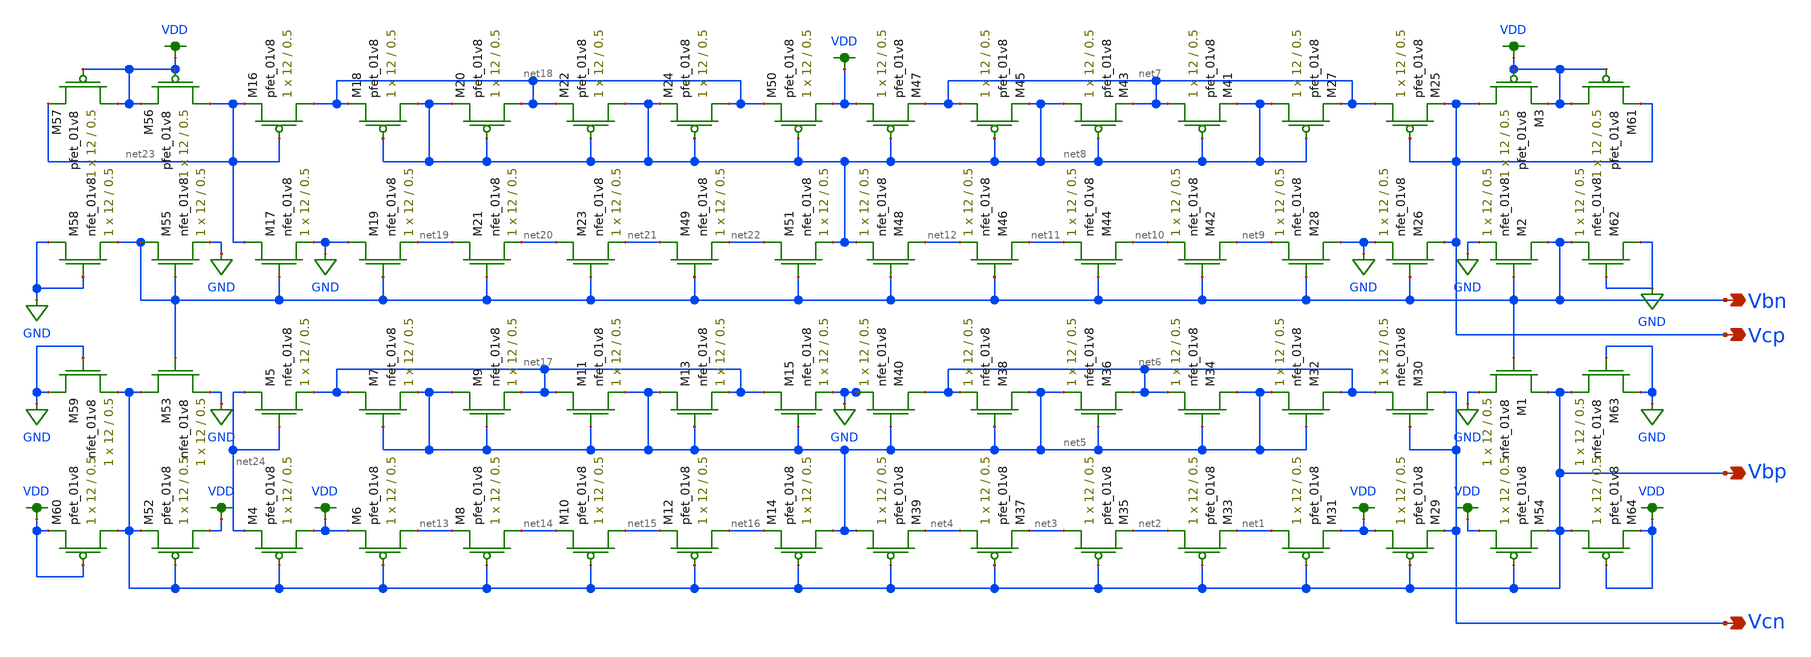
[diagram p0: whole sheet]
** sch_path: MP3/correction/xschem/v_gen_lds.sch
**.subckt v_gen_lds Vcp Vcn Vbn Vbp
*.opin Vcp
*.opin Vcn
*.opin Vbn
*.opin Vbp
XM29 VDD Vbp Vcn VDD sky130_fd_pr__pfet_01v8 L=0.5 W=12 nf=1 ad='int((nf+1)/2) * W/nf * 0.29' as='int((nf+2)/2) * W/nf * 0.29'
+ pd='2*int((nf+1)/2) * (W/nf + 0.29)' ps='2*int((nf+2)/2) * (W/nf + 0.29)' nrd='0.29 / W' nrs='0.29 / W'
+ sa=0 sb=0 sd=0 mult=1 m=1
XM30 Vcn Vcn net6 GND sky130_fd_pr__nfet_01v8 L=0.5 W=12 nf=1 ad='int((nf+1)/2) * W/nf * 0.29' as='int((nf+2)/2) * W/nf * 0.29'
+ pd='2*int((nf+1)/2) * (W/nf + 0.29)' ps='2*int((nf+2)/2) * (W/nf + 0.29)' nrd='0.29 / W' nrs='0.29 / W'
+ sa=0 sb=0 sd=0 mult=1 m=1
XM31 net1 Vbp VDD VDD sky130_fd_pr__pfet_01v8 L=0.5 W=12 nf=1 ad='int((nf+1)/2) * W/nf * 0.29' as='int((nf+2)/2) * W/nf * 0.29'
+ pd='2*int((nf+1)/2) * (W/nf + 0.29)' ps='2*int((nf+2)/2) * (W/nf + 0.29)' nrd='0.29 / W' nrs='0.29 / W'
+ sa=0 sb=0 sd=0 mult=1 m=1
XM32 net6 net5 net5 GND sky130_fd_pr__nfet_01v8 L=0.5 W=12 nf=1 ad='int((nf+1)/2) * W/nf * 0.29' as='int((nf+2)/2) * W/nf * 0.29'
+ pd='2*int((nf+1)/2) * (W/nf + 0.29)' ps='2*int((nf+2)/2) * (W/nf + 0.29)' nrd='0.29 / W' nrs='0.29 / W'
+ sa=0 sb=0 sd=0 mult=1 m=1
XM33 net2 Vbp net1 VDD sky130_fd_pr__pfet_01v8 L=0.5 W=12 nf=1 ad='int((nf+1)/2) * W/nf * 0.29' as='int((nf+2)/2) * W/nf * 0.29'
+ pd='2*int((nf+1)/2) * (W/nf + 0.29)' ps='2*int((nf+2)/2) * (W/nf + 0.29)' nrd='0.29 / W' nrs='0.29 / W'
+ sa=0 sb=0 sd=0 mult=1 m=1
XM34 net5 net5 net6 GND sky130_fd_pr__nfet_01v8 L=0.5 W=12 nf=1 ad='int((nf+1)/2) * W/nf * 0.29' as='int((nf+2)/2) * W/nf * 0.29'
+ pd='2*int((nf+1)/2) * (W/nf + 0.29)' ps='2*int((nf+2)/2) * (W/nf + 0.29)' nrd='0.29 / W' nrs='0.29 / W'
+ sa=0 sb=0 sd=0 mult=1 m=1
XM35 net3 Vbp net2 VDD sky130_fd_pr__pfet_01v8 L=0.5 W=12 nf=1 ad='int((nf+1)/2) * W/nf * 0.29' as='int((nf+2)/2) * W/nf * 0.29'
+ pd='2*int((nf+1)/2) * (W/nf + 0.29)' ps='2*int((nf+2)/2) * (W/nf + 0.29)' nrd='0.29 / W' nrs='0.29 / W'
+ sa=0 sb=0 sd=0 mult=1 m=1
XM36 net6 net5 net5 GND sky130_fd_pr__nfet_01v8 L=0.5 W=12 nf=1 ad='int((nf+1)/2) * W/nf * 0.29' as='int((nf+2)/2) * W/nf * 0.29'
+ pd='2*int((nf+1)/2) * (W/nf + 0.29)' ps='2*int((nf+2)/2) * (W/nf + 0.29)' nrd='0.29 / W' nrs='0.29 / W'
+ sa=0 sb=0 sd=0 mult=1 m=1
XM37 net4 Vbp net3 VDD sky130_fd_pr__pfet_01v8 L=0.5 W=12 nf=1 ad='int((nf+1)/2) * W/nf * 0.29' as='int((nf+2)/2) * W/nf * 0.29'
+ pd='2*int((nf+1)/2) * (W/nf + 0.29)' ps='2*int((nf+2)/2) * (W/nf + 0.29)' nrd='0.29 / W' nrs='0.29 / W'
+ sa=0 sb=0 sd=0 mult=1 m=1
XM38 net5 net5 net6 GND sky130_fd_pr__nfet_01v8 L=0.5 W=12 nf=1 ad='int((nf+1)/2) * W/nf * 0.29' as='int((nf+2)/2) * W/nf * 0.29'
+ pd='2*int((nf+1)/2) * (W/nf + 0.29)' ps='2*int((nf+2)/2) * (W/nf + 0.29)' nrd='0.29 / W' nrs='0.29 / W'
+ sa=0 sb=0 sd=0 mult=1 m=1
XM39 net5 Vbp net4 VDD sky130_fd_pr__pfet_01v8 L=0.5 W=12 nf=1 ad='int((nf+1)/2) * W/nf * 0.29' as='int((nf+2)/2) * W/nf * 0.29'
+ pd='2*int((nf+1)/2) * (W/nf + 0.29)' ps='2*int((nf+2)/2) * (W/nf + 0.29)' nrd='0.29 / W' nrs='0.29 / W'
+ sa=0 sb=0 sd=0 mult=1 m=1
XM40 net6 net5 GND GND sky130_fd_pr__nfet_01v8 L=0.5 W=12 nf=1 ad='int((nf+1)/2) * W/nf * 0.29' as='int((nf+2)/2) * W/nf * 0.29'
+ pd='2*int((nf+1)/2) * (W/nf + 0.29)' ps='2*int((nf+2)/2) * (W/nf + 0.29)' nrd='0.29 / W' nrs='0.29 / W'
+ sa=0 sb=0 sd=0 mult=1 m=1
XM25 net7 Vcp Vcp VDD sky130_fd_pr__pfet_01v8 L=0.5 W=12 nf=1 ad='int((nf+1)/2) * W/nf * 0.29' as='int((nf+2)/2) * W/nf * 0.29'
+ pd='2*int((nf+1)/2) * (W/nf + 0.29)' ps='2*int((nf+2)/2) * (W/nf + 0.29)' nrd='0.29 / W' nrs='0.29 / W'
+ sa=0 sb=0 sd=0 mult=1 m=1
XM26 Vcp Vbn GND GND sky130_fd_pr__nfet_01v8 L=0.5 W=12 nf=1 ad='int((nf+1)/2) * W/nf * 0.29' as='int((nf+2)/2) * W/nf * 0.29'
+ pd='2*int((nf+1)/2) * (W/nf + 0.29)' ps='2*int((nf+2)/2) * (W/nf + 0.29)' nrd='0.29 / W' nrs='0.29 / W'
+ sa=0 sb=0 sd=0 mult=1 m=1
XM27 net8 net8 net7 VDD sky130_fd_pr__pfet_01v8 L=0.5 W=12 nf=1 ad='int((nf+1)/2) * W/nf * 0.29' as='int((nf+2)/2) * W/nf * 0.29'
+ pd='2*int((nf+1)/2) * (W/nf + 0.29)' ps='2*int((nf+2)/2) * (W/nf + 0.29)' nrd='0.29 / W' nrs='0.29 / W'
+ sa=0 sb=0 sd=0 mult=1 m=1
XM28 GND Vbn net9 GND sky130_fd_pr__nfet_01v8 L=0.5 W=12 nf=1 ad='int((nf+1)/2) * W/nf * 0.29' as='int((nf+2)/2) * W/nf * 0.29'
+ pd='2*int((nf+1)/2) * (W/nf + 0.29)' ps='2*int((nf+2)/2) * (W/nf + 0.29)' nrd='0.29 / W' nrs='0.29 / W'
+ sa=0 sb=0 sd=0 mult=1 m=1
XM41 net7 net8 net8 VDD sky130_fd_pr__pfet_01v8 L=0.5 W=12 nf=1 ad='int((nf+1)/2) * W/nf * 0.29' as='int((nf+2)/2) * W/nf * 0.29'
+ pd='2*int((nf+1)/2) * (W/nf + 0.29)' ps='2*int((nf+2)/2) * (W/nf + 0.29)' nrd='0.29 / W' nrs='0.29 / W'
+ sa=0 sb=0 sd=0 mult=1 m=1
XM42 net9 Vbn net10 GND sky130_fd_pr__nfet_01v8 L=0.5 W=12 nf=1 ad='int((nf+1)/2) * W/nf * 0.29' as='int((nf+2)/2) * W/nf * 0.29'
+ pd='2*int((nf+1)/2) * (W/nf + 0.29)' ps='2*int((nf+2)/2) * (W/nf + 0.29)' nrd='0.29 / W' nrs='0.29 / W'
+ sa=0 sb=0 sd=0 mult=1 m=1
XM43 net8 net8 net7 VDD sky130_fd_pr__pfet_01v8 L=0.5 W=12 nf=1 ad='int((nf+1)/2) * W/nf * 0.29' as='int((nf+2)/2) * W/nf * 0.29'
+ pd='2*int((nf+1)/2) * (W/nf + 0.29)' ps='2*int((nf+2)/2) * (W/nf + 0.29)' nrd='0.29 / W' nrs='0.29 / W'
+ sa=0 sb=0 sd=0 mult=1 m=1
XM44 net10 Vbn net11 GND sky130_fd_pr__nfet_01v8 L=0.5 W=12 nf=1 ad='int((nf+1)/2) * W/nf * 0.29' as='int((nf+2)/2) * W/nf * 0.29'
+ pd='2*int((nf+1)/2) * (W/nf + 0.29)' ps='2*int((nf+2)/2) * (W/nf + 0.29)' nrd='0.29 / W' nrs='0.29 / W'
+ sa=0 sb=0 sd=0 mult=1 m=1
XM45 net7 net8 net8 VDD sky130_fd_pr__pfet_01v8 L=0.5 W=12 nf=1 ad='int((nf+1)/2) * W/nf * 0.29' as='int((nf+2)/2) * W/nf * 0.29'
+ pd='2*int((nf+1)/2) * (W/nf + 0.29)' ps='2*int((nf+2)/2) * (W/nf + 0.29)' nrd='0.29 / W' nrs='0.29 / W'
+ sa=0 sb=0 sd=0 mult=1 m=1
XM46 net11 Vbn net12 GND sky130_fd_pr__nfet_01v8 L=0.5 W=12 nf=1 ad='int((nf+1)/2) * W/nf * 0.29' as='int((nf+2)/2) * W/nf * 0.29'
+ pd='2*int((nf+1)/2) * (W/nf + 0.29)' ps='2*int((nf+2)/2) * (W/nf + 0.29)' nrd='0.29 / W' nrs='0.29 / W'
+ sa=0 sb=0 sd=0 mult=1 m=1
XM47 VDD net8 net7 VDD sky130_fd_pr__pfet_01v8 L=0.5 W=12 nf=1 ad='int((nf+1)/2) * W/nf * 0.29' as='int((nf+2)/2) * W/nf * 0.29'
+ pd='2*int((nf+1)/2) * (W/nf + 0.29)' ps='2*int((nf+2)/2) * (W/nf + 0.29)' nrd='0.29 / W' nrs='0.29 / W'
+ sa=0 sb=0 sd=0 mult=1 m=1
XM48 net12 Vbn net8 GND sky130_fd_pr__nfet_01v8 L=0.5 W=12 nf=1 ad='int((nf+1)/2) * W/nf * 0.29' as='int((nf+2)/2) * W/nf * 0.29'
+ pd='2*int((nf+1)/2) * (W/nf + 0.29)' ps='2*int((nf+2)/2) * (W/nf + 0.29)' nrd='0.29 / W' nrs='0.29 / W'
+ sa=0 sb=0 sd=0 mult=1 m=1
XM54 VDD Vbp Vbp VDD sky130_fd_pr__pfet_01v8 L=0.5 W=12 nf=1 ad='int((nf+1)/2) * W/nf * 0.29' as='int((nf+2)/2) * W/nf * 0.29'
+ pd='2*int((nf+1)/2) * (W/nf + 0.29)' ps='2*int((nf+2)/2) * (W/nf + 0.29)' nrd='0.29 / W' nrs='0.29 / W'
+ sa=0 sb=0 sd=0 mult=1 m=1
XM1 Vbp Vbn GND GND sky130_fd_pr__nfet_01v8 L=0.5 W=12 nf=1 ad='int((nf+1)/2) * W/nf * 0.29' as='int((nf+2)/2) * W/nf * 0.29'
+ pd='2*int((nf+1)/2) * (W/nf + 0.29)' ps='2*int((nf+2)/2) * (W/nf + 0.29)' nrd='0.29 / W' nrs='0.29 / W'
+ sa=0 sb=0 sd=0 mult=1 m=1
XM2 Vbn Vbn GND GND sky130_fd_pr__nfet_01v8 L=0.5 W=12 nf=1 ad='int((nf+1)/2) * W/nf * 0.29' as='int((nf+2)/2) * W/nf * 0.29'
+ pd='2*int((nf+1)/2) * (W/nf + 0.29)' ps='2*int((nf+2)/2) * (W/nf + 0.29)' nrd='0.29 / W' nrs='0.29 / W'
+ sa=0 sb=0 sd=0 mult=1 m=1
XM3 Vcp VDD VDD VDD sky130_fd_pr__pfet_01v8 L=0.5 W=12 nf=1 ad='int((nf+1)/2) * W/nf * 0.29' as='int((nf+2)/2) * W/nf * 0.29'
+ pd='2*int((nf+1)/2) * (W/nf + 0.29)' ps='2*int((nf+2)/2) * (W/nf + 0.29)' nrd='0.29 / W' nrs='0.29 / W'
+ sa=0 sb=0 sd=0 mult=1 m=1
XM4 VDD Vbp net24 VDD sky130_fd_pr__pfet_01v8 L=0.5 W=12 nf=1 ad='int((nf+1)/2) * W/nf * 0.29' as='int((nf+2)/2) * W/nf * 0.29'
+ pd='2*int((nf+1)/2) * (W/nf + 0.29)' ps='2*int((nf+2)/2) * (W/nf + 0.29)' nrd='0.29 / W' nrs='0.29 / W'
+ sa=0 sb=0 sd=0 mult=1 m=1
XM5 net24 net24 net17 GND sky130_fd_pr__nfet_01v8 L=0.5 W=12 nf=1 ad='int((nf+1)/2) * W/nf * 0.29' as='int((nf+2)/2) * W/nf * 0.29'
+ pd='2*int((nf+1)/2) * (W/nf + 0.29)' ps='2*int((nf+2)/2) * (W/nf + 0.29)' nrd='0.29 / W' nrs='0.29 / W'
+ sa=0 sb=0 sd=0 mult=1 m=1
XM6 net13 Vbp VDD VDD sky130_fd_pr__pfet_01v8 L=0.5 W=12 nf=1 ad='int((nf+1)/2) * W/nf * 0.29' as='int((nf+2)/2) * W/nf * 0.29'
+ pd='2*int((nf+1)/2) * (W/nf + 0.29)' ps='2*int((nf+2)/2) * (W/nf + 0.29)' nrd='0.29 / W' nrs='0.29 / W'
+ sa=0 sb=0 sd=0 mult=1 m=1
XM7 net17 net5 net5 GND sky130_fd_pr__nfet_01v8 L=0.5 W=12 nf=1 ad='int((nf+1)/2) * W/nf * 0.29' as='int((nf+2)/2) * W/nf * 0.29'
+ pd='2*int((nf+1)/2) * (W/nf + 0.29)' ps='2*int((nf+2)/2) * (W/nf + 0.29)' nrd='0.29 / W' nrs='0.29 / W'
+ sa=0 sb=0 sd=0 mult=1 m=1
XM8 net14 Vbp net13 VDD sky130_fd_pr__pfet_01v8 L=0.5 W=12 nf=1 ad='int((nf+1)/2) * W/nf * 0.29' as='int((nf+2)/2) * W/nf * 0.29'
+ pd='2*int((nf+1)/2) * (W/nf + 0.29)' ps='2*int((nf+2)/2) * (W/nf + 0.29)' nrd='0.29 / W' nrs='0.29 / W'
+ sa=0 sb=0 sd=0 mult=1 m=1
XM9 net5 net5 net17 GND sky130_fd_pr__nfet_01v8 L=0.5 W=12 nf=1 ad='int((nf+1)/2) * W/nf * 0.29' as='int((nf+2)/2) * W/nf * 0.29'
+ pd='2*int((nf+1)/2) * (W/nf + 0.29)' ps='2*int((nf+2)/2) * (W/nf + 0.29)' nrd='0.29 / W' nrs='0.29 / W'
+ sa=0 sb=0 sd=0 mult=1 m=1
XM10 net15 Vbp net14 VDD sky130_fd_pr__pfet_01v8 L=0.5 W=12 nf=1 ad='int((nf+1)/2) * W/nf * 0.29' as='int((nf+2)/2) * W/nf * 0.29'
+ pd='2*int((nf+1)/2) * (W/nf + 0.29)' ps='2*int((nf+2)/2) * (W/nf + 0.29)' nrd='0.29 / W' nrs='0.29 / W'
+ sa=0 sb=0 sd=0 mult=1 m=1
XM11 net17 net5 net5 GND sky130_fd_pr__nfet_01v8 L=0.5 W=12 nf=1 ad='int((nf+1)/2) * W/nf * 0.29' as='int((nf+2)/2) * W/nf * 0.29'
+ pd='2*int((nf+1)/2) * (W/nf + 0.29)' ps='2*int((nf+2)/2) * (W/nf + 0.29)' nrd='0.29 / W' nrs='0.29 / W'
+ sa=0 sb=0 sd=0 mult=1 m=1
XM12 net16 Vbp net15 VDD sky130_fd_pr__pfet_01v8 L=0.5 W=12 nf=1 ad='int((nf+1)/2) * W/nf * 0.29' as='int((nf+2)/2) * W/nf * 0.29'
+ pd='2*int((nf+1)/2) * (W/nf + 0.29)' ps='2*int((nf+2)/2) * (W/nf + 0.29)' nrd='0.29 / W' nrs='0.29 / W'
+ sa=0 sb=0 sd=0 mult=1 m=1
XM13 net5 net5 net17 GND sky130_fd_pr__nfet_01v8 L=0.5 W=12 nf=1 ad='int((nf+1)/2) * W/nf * 0.29' as='int((nf+2)/2) * W/nf * 0.29'
+ pd='2*int((nf+1)/2) * (W/nf + 0.29)' ps='2*int((nf+2)/2) * (W/nf + 0.29)' nrd='0.29 / W' nrs='0.29 / W'
+ sa=0 sb=0 sd=0 mult=1 m=1
XM14 net5 Vbp net16 VDD sky130_fd_pr__pfet_01v8 L=0.5 W=12 nf=1 ad='int((nf+1)/2) * W/nf * 0.29' as='int((nf+2)/2) * W/nf * 0.29'
+ pd='2*int((nf+1)/2) * (W/nf + 0.29)' ps='2*int((nf+2)/2) * (W/nf + 0.29)' nrd='0.29 / W' nrs='0.29 / W'
+ sa=0 sb=0 sd=0 mult=1 m=1
XM15 net17 net5 GND GND sky130_fd_pr__nfet_01v8 L=0.5 W=12 nf=1 ad='int((nf+1)/2) * W/nf * 0.29' as='int((nf+2)/2) * W/nf * 0.29'
+ pd='2*int((nf+1)/2) * (W/nf + 0.29)' ps='2*int((nf+2)/2) * (W/nf + 0.29)' nrd='0.29 / W' nrs='0.29 / W'
+ sa=0 sb=0 sd=0 mult=1 m=1
XM16 net18 net23 net23 VDD sky130_fd_pr__pfet_01v8 L=0.5 W=12 nf=1 ad='int((nf+1)/2) * W/nf * 0.29' as='int((nf+2)/2) * W/nf * 0.29'
+ pd='2*int((nf+1)/2) * (W/nf + 0.29)' ps='2*int((nf+2)/2) * (W/nf + 0.29)' nrd='0.29 / W' nrs='0.29 / W'
+ sa=0 sb=0 sd=0 mult=1 m=1
XM17 net23 Vbn GND GND sky130_fd_pr__nfet_01v8 L=0.5 W=12 nf=1 ad='int((nf+1)/2) * W/nf * 0.29' as='int((nf+2)/2) * W/nf * 0.29'
+ pd='2*int((nf+1)/2) * (W/nf + 0.29)' ps='2*int((nf+2)/2) * (W/nf + 0.29)' nrd='0.29 / W' nrs='0.29 / W'
+ sa=0 sb=0 sd=0 mult=1 m=1
XM18 net8 net8 net18 VDD sky130_fd_pr__pfet_01v8 L=0.5 W=12 nf=1 ad='int((nf+1)/2) * W/nf * 0.29' as='int((nf+2)/2) * W/nf * 0.29'
+ pd='2*int((nf+1)/2) * (W/nf + 0.29)' ps='2*int((nf+2)/2) * (W/nf + 0.29)' nrd='0.29 / W' nrs='0.29 / W'
+ sa=0 sb=0 sd=0 mult=1 m=1
XM19 GND Vbn net19 GND sky130_fd_pr__nfet_01v8 L=0.5 W=12 nf=1 ad='int((nf+1)/2) * W/nf * 0.29' as='int((nf+2)/2) * W/nf * 0.29'
+ pd='2*int((nf+1)/2) * (W/nf + 0.29)' ps='2*int((nf+2)/2) * (W/nf + 0.29)' nrd='0.29 / W' nrs='0.29 / W'
+ sa=0 sb=0 sd=0 mult=1 m=1
XM20 net18 net8 net8 VDD sky130_fd_pr__pfet_01v8 L=0.5 W=12 nf=1 ad='int((nf+1)/2) * W/nf * 0.29' as='int((nf+2)/2) * W/nf * 0.29'
+ pd='2*int((nf+1)/2) * (W/nf + 0.29)' ps='2*int((nf+2)/2) * (W/nf + 0.29)' nrd='0.29 / W' nrs='0.29 / W'
+ sa=0 sb=0 sd=0 mult=1 m=1
XM21 net19 Vbn net20 GND sky130_fd_pr__nfet_01v8 L=0.5 W=12 nf=1 ad='int((nf+1)/2) * W/nf * 0.29' as='int((nf+2)/2) * W/nf * 0.29'
+ pd='2*int((nf+1)/2) * (W/nf + 0.29)' ps='2*int((nf+2)/2) * (W/nf + 0.29)' nrd='0.29 / W' nrs='0.29 / W'
+ sa=0 sb=0 sd=0 mult=1 m=1
XM22 net8 net8 net18 VDD sky130_fd_pr__pfet_01v8 L=0.5 W=12 nf=1 ad='int((nf+1)/2) * W/nf * 0.29' as='int((nf+2)/2) * W/nf * 0.29'
+ pd='2*int((nf+1)/2) * (W/nf + 0.29)' ps='2*int((nf+2)/2) * (W/nf + 0.29)' nrd='0.29 / W' nrs='0.29 / W'
+ sa=0 sb=0 sd=0 mult=1 m=1
XM23 net20 Vbn net21 GND sky130_fd_pr__nfet_01v8 L=0.5 W=12 nf=1 ad='int((nf+1)/2) * W/nf * 0.29' as='int((nf+2)/2) * W/nf * 0.29'
+ pd='2*int((nf+1)/2) * (W/nf + 0.29)' ps='2*int((nf+2)/2) * (W/nf + 0.29)' nrd='0.29 / W' nrs='0.29 / W'
+ sa=0 sb=0 sd=0 mult=1 m=1
XM24 net18 net8 net8 VDD sky130_fd_pr__pfet_01v8 L=0.5 W=12 nf=1 ad='int((nf+1)/2) * W/nf * 0.29' as='int((nf+2)/2) * W/nf * 0.29'
+ pd='2*int((nf+1)/2) * (W/nf + 0.29)' ps='2*int((nf+2)/2) * (W/nf + 0.29)' nrd='0.29 / W' nrs='0.29 / W'
+ sa=0 sb=0 sd=0 mult=1 m=1
XM49 net21 Vbn net22 GND sky130_fd_pr__nfet_01v8 L=0.5 W=12 nf=1 ad='int((nf+1)/2) * W/nf * 0.29' as='int((nf+2)/2) * W/nf * 0.29'
+ pd='2*int((nf+1)/2) * (W/nf + 0.29)' ps='2*int((nf+2)/2) * (W/nf + 0.29)' nrd='0.29 / W' nrs='0.29 / W'
+ sa=0 sb=0 sd=0 mult=1 m=1
XM50 VDD net8 net18 VDD sky130_fd_pr__pfet_01v8 L=0.5 W=12 nf=1 ad='int((nf+1)/2) * W/nf * 0.29' as='int((nf+2)/2) * W/nf * 0.29'
+ pd='2*int((nf+1)/2) * (W/nf + 0.29)' ps='2*int((nf+2)/2) * (W/nf + 0.29)' nrd='0.29 / W' nrs='0.29 / W'
+ sa=0 sb=0 sd=0 mult=1 m=1
XM51 net22 Vbn net8 GND sky130_fd_pr__nfet_01v8 L=0.5 W=12 nf=1 ad='int((nf+1)/2) * W/nf * 0.29' as='int((nf+2)/2) * W/nf * 0.29'
+ pd='2*int((nf+1)/2) * (W/nf + 0.29)' ps='2*int((nf+2)/2) * (W/nf + 0.29)' nrd='0.29 / W' nrs='0.29 / W'
+ sa=0 sb=0 sd=0 mult=1 m=1
XM52 VDD Vbp Vbp VDD sky130_fd_pr__pfet_01v8 L=0.5 W=12 nf=1 ad='int((nf+1)/2) * W/nf * 0.29' as='int((nf+2)/2) * W/nf * 0.29'
+ pd='2*int((nf+1)/2) * (W/nf + 0.29)' ps='2*int((nf+2)/2) * (W/nf + 0.29)' nrd='0.29 / W' nrs='0.29 / W'
+ sa=0 sb=0 sd=0 mult=1 m=1
XM53 Vbp Vbn GND GND sky130_fd_pr__nfet_01v8 L=0.5 W=12 nf=1 ad='int((nf+1)/2) * W/nf * 0.29' as='int((nf+2)/2) * W/nf * 0.29'
+ pd='2*int((nf+1)/2) * (W/nf + 0.29)' ps='2*int((nf+2)/2) * (W/nf + 0.29)' nrd='0.29 / W' nrs='0.29 / W'
+ sa=0 sb=0 sd=0 mult=1 m=1
XM55 Vbn Vbn GND GND sky130_fd_pr__nfet_01v8 L=0.5 W=12 nf=1 ad='int((nf+1)/2) * W/nf * 0.29' as='int((nf+2)/2) * W/nf * 0.29'
+ pd='2*int((nf+1)/2) * (W/nf + 0.29)' ps='2*int((nf+2)/2) * (W/nf + 0.29)' nrd='0.29 / W' nrs='0.29 / W'
+ sa=0 sb=0 sd=0 mult=1 m=1
XM56 net23 VDD VDD VDD sky130_fd_pr__pfet_01v8 L=0.5 W=12 nf=1 ad='int((nf+1)/2) * W/nf * 0.29' as='int((nf+2)/2) * W/nf * 0.29'
+ pd='2*int((nf+1)/2) * (W/nf + 0.29)' ps='2*int((nf+2)/2) * (W/nf + 0.29)' nrd='0.29 / W' nrs='0.29 / W'
+ sa=0 sb=0 sd=0 mult=1 m=1
XM57 VDD VDD net23 VDD sky130_fd_pr__pfet_01v8 L=0.5 W=12 nf=1 ad='int((nf+1)/2) * W/nf * 0.29' as='int((nf+2)/2) * W/nf * 0.29'
+ pd='2*int((nf+1)/2) * (W/nf + 0.29)' ps='2*int((nf+2)/2) * (W/nf + 0.29)' nrd='0.29 / W' nrs='0.29 / W'
+ sa=0 sb=0 sd=0 mult=1 m=1
XM58 GND GND Vbn GND sky130_fd_pr__nfet_01v8 L=0.5 W=12 nf=1 ad='int((nf+1)/2) * W/nf * 0.29' as='int((nf+2)/2) * W/nf * 0.29'
+ pd='2*int((nf+1)/2) * (W/nf + 0.29)' ps='2*int((nf+2)/2) * (W/nf + 0.29)' nrd='0.29 / W' nrs='0.29 / W'
+ sa=0 sb=0 sd=0 mult=1 m=1
XM59 GND GND Vbp GND sky130_fd_pr__nfet_01v8 L=0.5 W=12 nf=1 ad='int((nf+1)/2) * W/nf * 0.29' as='int((nf+2)/2) * W/nf * 0.29'
+ pd='2*int((nf+1)/2) * (W/nf + 0.29)' ps='2*int((nf+2)/2) * (W/nf + 0.29)' nrd='0.29 / W' nrs='0.29 / W'
+ sa=0 sb=0 sd=0 mult=1 m=1
XM60 Vbp VDD VDD VDD sky130_fd_pr__pfet_01v8 L=0.5 W=12 nf=1 ad='int((nf+1)/2) * W/nf * 0.29' as='int((nf+2)/2) * W/nf * 0.29'
+ pd='2*int((nf+1)/2) * (W/nf + 0.29)' ps='2*int((nf+2)/2) * (W/nf + 0.29)' nrd='0.29 / W' nrs='0.29 / W'
+ sa=0 sb=0 sd=0 mult=1 m=1
XM61 VDD VDD Vcp VDD sky130_fd_pr__pfet_01v8 L=0.5 W=12 nf=1 ad='int((nf+1)/2) * W/nf * 0.29' as='int((nf+2)/2) * W/nf * 0.29'
+ pd='2*int((nf+1)/2) * (W/nf + 0.29)' ps='2*int((nf+2)/2) * (W/nf + 0.29)' nrd='0.29 / W' nrs='0.29 / W'
+ sa=0 sb=0 sd=0 mult=1 m=1
XM62 GND GND Vbn GND sky130_fd_pr__nfet_01v8 L=0.5 W=12 nf=1 ad='int((nf+1)/2) * W/nf * 0.29' as='int((nf+2)/2) * W/nf * 0.29'
+ pd='2*int((nf+1)/2) * (W/nf + 0.29)' ps='2*int((nf+2)/2) * (W/nf + 0.29)' nrd='0.29 / W' nrs='0.29 / W'
+ sa=0 sb=0 sd=0 mult=1 m=1
XM63 GND GND Vbp GND sky130_fd_pr__nfet_01v8 L=0.5 W=12 nf=1 ad='int((nf+1)/2) * W/nf * 0.29' as='int((nf+2)/2) * W/nf * 0.29'
+ pd='2*int((nf+1)/2) * (W/nf + 0.29)' ps='2*int((nf+2)/2) * (W/nf + 0.29)' nrd='0.29 / W' nrs='0.29 / W'
+ sa=0 sb=0 sd=0 mult=1 m=1
XM64 Vbp VDD VDD VDD sky130_fd_pr__pfet_01v8 L=0.5 W=12 nf=1 ad='int((nf+1)/2) * W/nf * 0.29' as='int((nf+2)/2) * W/nf * 0.29'
+ pd='2*int((nf+1)/2) * (W/nf + 0.29)' ps='2*int((nf+2)/2) * (W/nf + 0.29)' nrd='0.29 / W' nrs='0.29 / W'
+ sa=0 sb=0 sd=0 mult=1 m=1
**.ends
.GLOBAL VDD
.GLOBAL GND
.end
